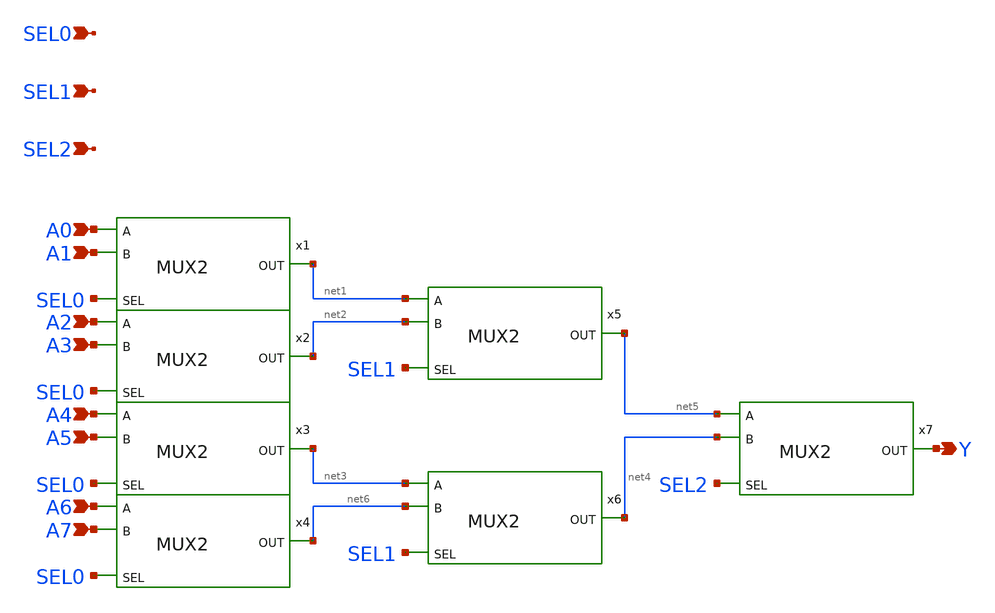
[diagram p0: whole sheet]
** sch_path: design/xschem/MUX/MUX8.sch
**.subckt MUX8 A0 Y A1 A2 A3 A4 A5 A6 A7 SEL0 SEL1 SEL2
*.ipin A0
*.opin Y
*.ipin A1
*.ipin A2
*.ipin A3
*.ipin A4
*.ipin A5
*.ipin A6
*.ipin A7
*.ipin SEL0
*.ipin SEL1
*.ipin SEL2
x1 A0 A1 SEL0 net1 VSS VDD MUX2
x2 A2 A3 SEL0 net2 VSS VDD MUX2
x3 A4 A5 SEL0 net3 VSS VDD MUX2
x4 A6 A7 SEL0 net6 VSS VDD MUX2
x5 net1 net2 SEL1 net5 VSS VDD MUX2
x6 net3 net6 SEL1 net4 VSS VDD MUX2
x7 net5 net4 SEL2 Y VSS VDD MUX2
**.ends

* expanding   symbol:  MUX/MUX2.sym # of pins=4
** sym_path: design/xschem/MUX/MUX2.sym
** sch_path: design/xschem/MUX/MUX2.sch
.subckt MUX2 A B SEL OUT VSS VDD
*.ipin A
*.ipin B
*.ipin SEL
*.opin OUT
x1 A B SEL !SEL OUT A !SEL B SEL VSS VDD cg4
x2 SEL VSS VDD !SEL inv
.ends


* expanding   symbol:  CG4/cg4.sym # of pins=9
** sym_path: design/xschem/CG4/cg4.sym
** sch_path: design/xschem/CG4/cg4.sch
.subckt cg4 P3 P4 P2 P1 OUT N2 N1 N4 N3 VSS VDD
*.ipin P3
*.ipin P1
*.ipin N1
*.ipin N3
*.ipin P4
*.ipin P2
*.ipin N2
*.ipin N4
*.opin OUT
XM1 OUT N1 net1 VSS sky130_fd_pr__nfet_01v8 L=0.15 W=2 nf=1 ad='int((nf+1)/2) * W/nf * 0.29' as='int((nf+2)/2) * W/nf * 0.29'
+ pd='2*int((nf+1)/2) * (W/nf + 0.29)' ps='2*int((nf+2)/2) * (W/nf + 0.29)' nrd='0.29 / W' nrs='0.29 / W'
+ sa=0 sb=0 sd=0 mult=1 m=1
XM2 OUT N2 net2 VSS sky130_fd_pr__nfet_01v8 L=0.15 W=2 nf=1 ad='int((nf+1)/2) * W/nf * 0.29' as='int((nf+2)/2) * W/nf * 0.29'
+ pd='2*int((nf+1)/2) * (W/nf + 0.29)' ps='2*int((nf+2)/2) * (W/nf + 0.29)' nrd='0.29 / W' nrs='0.29 / W'
+ sa=0 sb=0 sd=0 mult=1 m=1
XM3 net1 N3 VSS VSS sky130_fd_pr__nfet_01v8 L=0.15 W=2 nf=1 ad='int((nf+1)/2) * W/nf * 0.29' as='int((nf+2)/2) * W/nf * 0.29'
+ pd='2*int((nf+1)/2) * (W/nf + 0.29)' ps='2*int((nf+2)/2) * (W/nf + 0.29)' nrd='0.29 / W' nrs='0.29 / W'
+ sa=0 sb=0 sd=0 mult=1 m=1
XM4 net2 N4 VSS VSS sky130_fd_pr__nfet_01v8 L=0.15 W=2 nf=1 ad='int((nf+1)/2) * W/nf * 0.29' as='int((nf+2)/2) * W/nf * 0.29'
+ pd='2*int((nf+1)/2) * (W/nf + 0.29)' ps='2*int((nf+2)/2) * (W/nf + 0.29)' nrd='0.29 / W' nrs='0.29 / W'
+ sa=0 sb=0 sd=0 mult=1 m=1
XM5 OUT P1 net3 VDD sky130_fd_pr__pfet_01v8 L=0.15 W=8.25 nf=1 ad='int((nf+1)/2) * W/nf * 0.29' as='int((nf+2)/2) * W/nf * 0.29'
+ pd='2*int((nf+1)/2) * (W/nf + 0.29)' ps='2*int((nf+2)/2) * (W/nf + 0.29)' nrd='0.29 / W' nrs='0.29 / W'
+ sa=0 sb=0 sd=0 mult=1 m=1
XM6 OUT P2 net3 VDD sky130_fd_pr__pfet_01v8 L=0.15 W=8.25 nf=1 ad='int((nf+1)/2) * W/nf * 0.29' as='int((nf+2)/2) * W/nf * 0.29'
+ pd='2*int((nf+1)/2) * (W/nf + 0.29)' ps='2*int((nf+2)/2) * (W/nf + 0.29)' nrd='0.29 / W' nrs='0.29 / W'
+ sa=0 sb=0 sd=0 mult=1 m=1
XM7 net3 P3 VDD VDD sky130_fd_pr__pfet_01v8 L=0.15 W=8.25 nf=1 ad='int((nf+1)/2) * W/nf * 0.29' as='int((nf+2)/2) * W/nf * 0.29'
+ pd='2*int((nf+1)/2) * (W/nf + 0.29)' ps='2*int((nf+2)/2) * (W/nf + 0.29)' nrd='0.29 / W' nrs='0.29 / W'
+ sa=0 sb=0 sd=0 mult=1 m=1
XM8 net3 P4 VDD VDD sky130_fd_pr__pfet_01v8 L=0.15 W=8.25 nf=1 ad='int((nf+1)/2) * W/nf * 0.29' as='int((nf+2)/2) * W/nf * 0.29'
+ pd='2*int((nf+1)/2) * (W/nf + 0.29)' ps='2*int((nf+2)/2) * (W/nf + 0.29)' nrd='0.29 / W' nrs='0.29 / W'
+ sa=0 sb=0 sd=0 mult=1 m=1
.ends


* expanding   symbol:  INV/inv.sym # of pins=2
** sym_path: design/xschem/INV/inv.sym
** sch_path: design/xschem/INV/inv.sch
.subckt inv A VSS VDD Y
*.ipin A
*.opin Y
XM2 Y A VSS GND sky130_fd_pr__nfet_01v8 L=0.15 W=1 nf=1 ad='int((nf+1)/2) * W/nf * 0.29' as='int((nf+2)/2) * W/nf * 0.29'
+ pd='2*int((nf+1)/2) * (W/nf + 0.29)' ps='2*int((nf+2)/2) * (W/nf + 0.29)' nrd='0.29 / W' nrs='0.29 / W'
+ sa=0 sb=0 sd=0 mult=1 m=1
XM1 Y A VDD VDD sky130_fd_pr__pfet_01v8 L=0.15 W=3.21 nf=1 ad='int((nf+1)/2) * W/nf * 0.29' as='int((nf+2)/2) * W/nf * 0.29'
+ pd='2*int((nf+1)/2) * (W/nf + 0.29)' ps='2*int((nf+2)/2) * (W/nf + 0.29)' nrd='0.29 / W' nrs='0.29 / W'
+ sa=0 sb=0 sd=0 mult=1 m=1
.ends

.end
